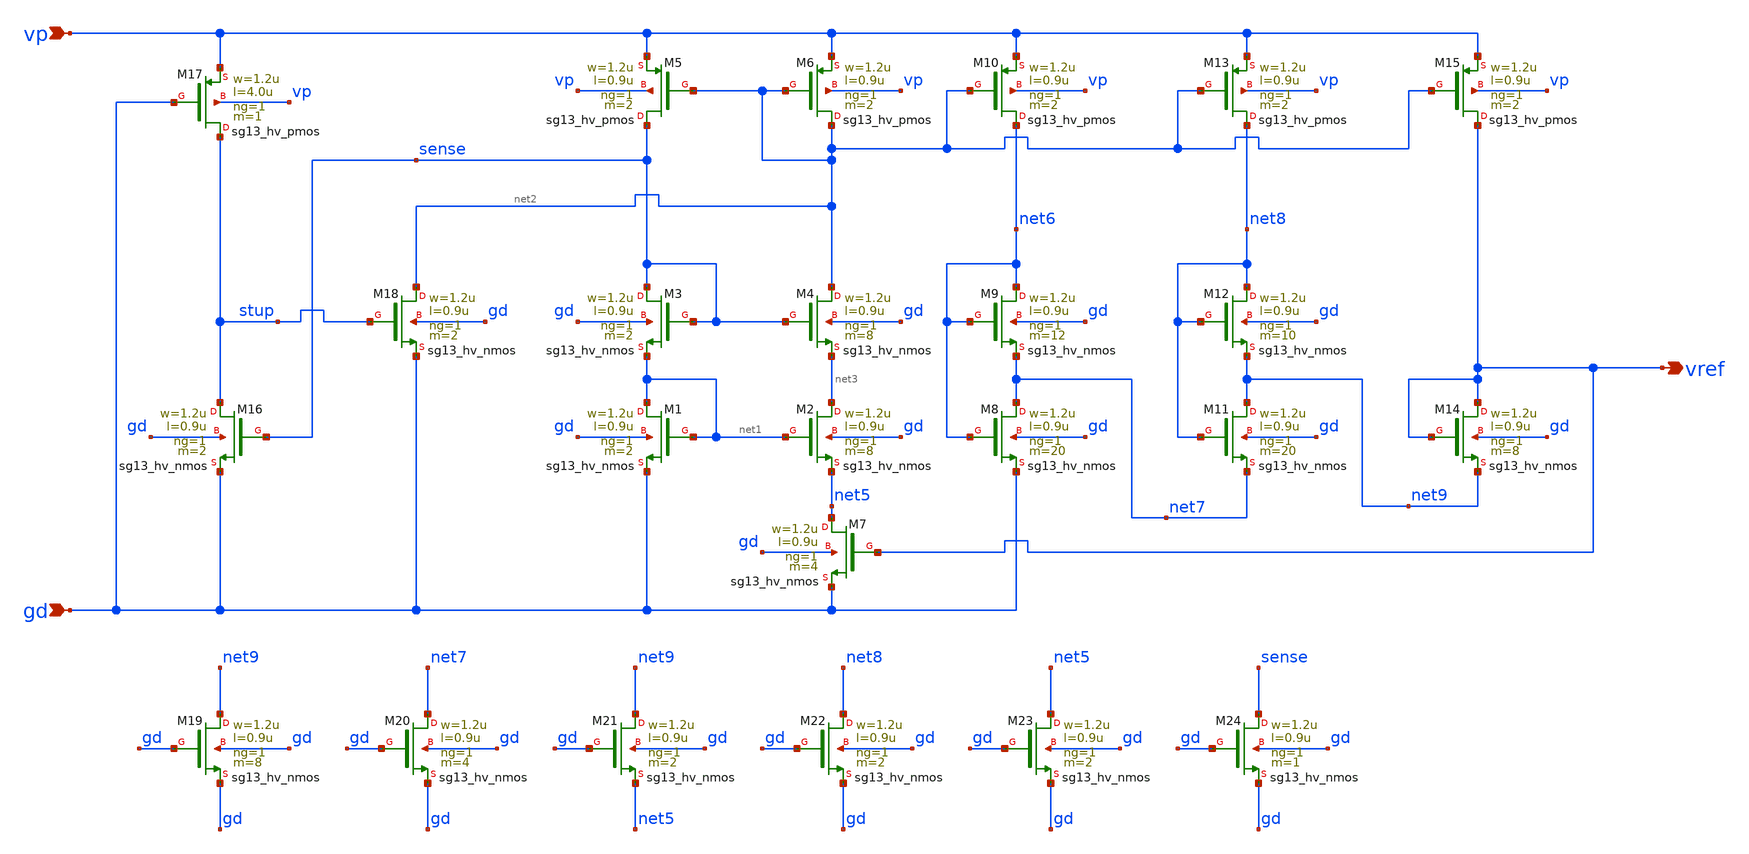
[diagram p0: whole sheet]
** sch_path: schematics/bandgap/bandgap_selfbias_core.sch
**.subckt bandgap_selfbias_core gd vp vref
*.ipin gd
*.ipin vp
*.opin vref
XM1 net1 net1 gd gd sg13_hv_nmos w=1.2u l=0.9u ng=1 m=2 mm_ok=1
XM2 net3 net1 net5 gd sg13_hv_nmos w=1.2u l=0.9u ng=1 m=8 mm_ok=1
XM7 net5 vref gd gd sg13_hv_nmos w=1.2u l=0.9u ng=1 m=4 mm_ok=1
XM3 sense sense net1 gd sg13_hv_nmos w=1.2u l=0.9u ng=1 m=2 mm_ok=1
XM4 net2 sense net3 gd sg13_hv_nmos w=1.2u l=0.9u ng=1 m=8 mm_ok=1
XM6 net2 net2 vp vp sg13_hv_pmos w=1.2u l=0.9u ng=1 m=2 mm_ok=1
XM5 sense net2 vp vp sg13_hv_pmos w=1.2u l=0.9u ng=1 m=2 mm_ok=1
XM10 net6 net2 vp vp sg13_hv_pmos w=1.2u l=0.9u ng=1 m=2 mm_ok=1
XM8 net7 net6 gd gd sg13_hv_nmos w=1.2u l=0.9u ng=1 m=20 mm_ok=1
XM9 net6 net6 net7 gd sg13_hv_nmos w=1.2u l=0.9u ng=1 m=12 mm_ok=1
XM13 net8 net2 vp vp sg13_hv_pmos w=1.2u l=0.9u ng=1 m=2 mm_ok=1
XM11 net9 net8 net7 gd sg13_hv_nmos w=1.2u l=0.9u ng=1 m=20 mm_ok=1
XM12 net8 net8 net9 gd sg13_hv_nmos w=1.2u l=0.9u ng=1 m=10 mm_ok=1
XM14 vref vref net9 gd sg13_hv_nmos w=1.2u l=0.9u ng=1 m=8 mm_ok=1
XM15 vref net2 vp vp sg13_hv_pmos w=1.2u l=0.9u ng=1 m=2 mm_ok=1
XM16 stup sense gd gd sg13_hv_nmos w=1.2u l=0.9u ng=1 m=2 mm_ok=1
XM17 stup gd vp vp sg13_hv_pmos w=1.2u l=4.0u ng=1 m=1 mm_ok=1
XM18 net2 stup gd gd sg13_hv_nmos w=1.2u l=0.9u ng=1 m=2 mm_ok=1
XM19 net9 gd gd gd sg13_hv_nmos w=1.2u l=0.9u ng=1 m=8 mm_ok=1
XM20 net7 gd gd gd sg13_hv_nmos w=1.2u l=0.9u ng=1 m=4 mm_ok=1
XM21 net9 gd net5 gd sg13_hv_nmos w=1.2u l=0.9u ng=1 m=2 mm_ok=1
XM22 net8 gd gd gd sg13_hv_nmos w=1.2u l=0.9u ng=1 m=2 mm_ok=1
XM23 net5 gd gd gd sg13_hv_nmos w=1.2u l=0.9u ng=1 m=2 mm_ok=1
XM24 sense gd gd gd sg13_hv_nmos w=1.2u l=0.9u ng=1 m=1 mm_ok=1
**.ends
.end
